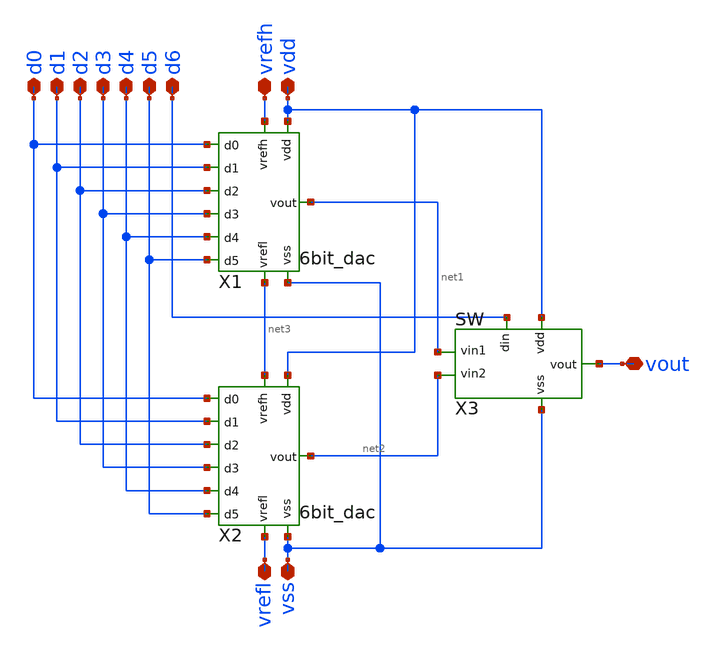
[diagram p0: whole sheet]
** sch_path: dac/1.schematics/untitled-3.sch
**.subckt untitled-3 vdd vss vrefh vrefl d0 d1 d2 d3 d4 d5 d6 vout
*.iopin vdd
*.iopin vss
*.iopin vrefh
*.iopin vrefl
*.iopin d0
*.iopin d1
*.iopin d2
*.iopin d3
*.iopin d4
*.iopin d5
*.iopin d6
*.iopin vout
X1 vdd vss vrefh net3 d0 d1 d2 d3 d4 d5 net1 6bit_dac
X2 vdd vss net3 vrefl d0 d1 d2 d3 d4 d5 net2 6bit_dac
X3 vdd vss d6 net1 net2 vout sw
**.ends
.end
